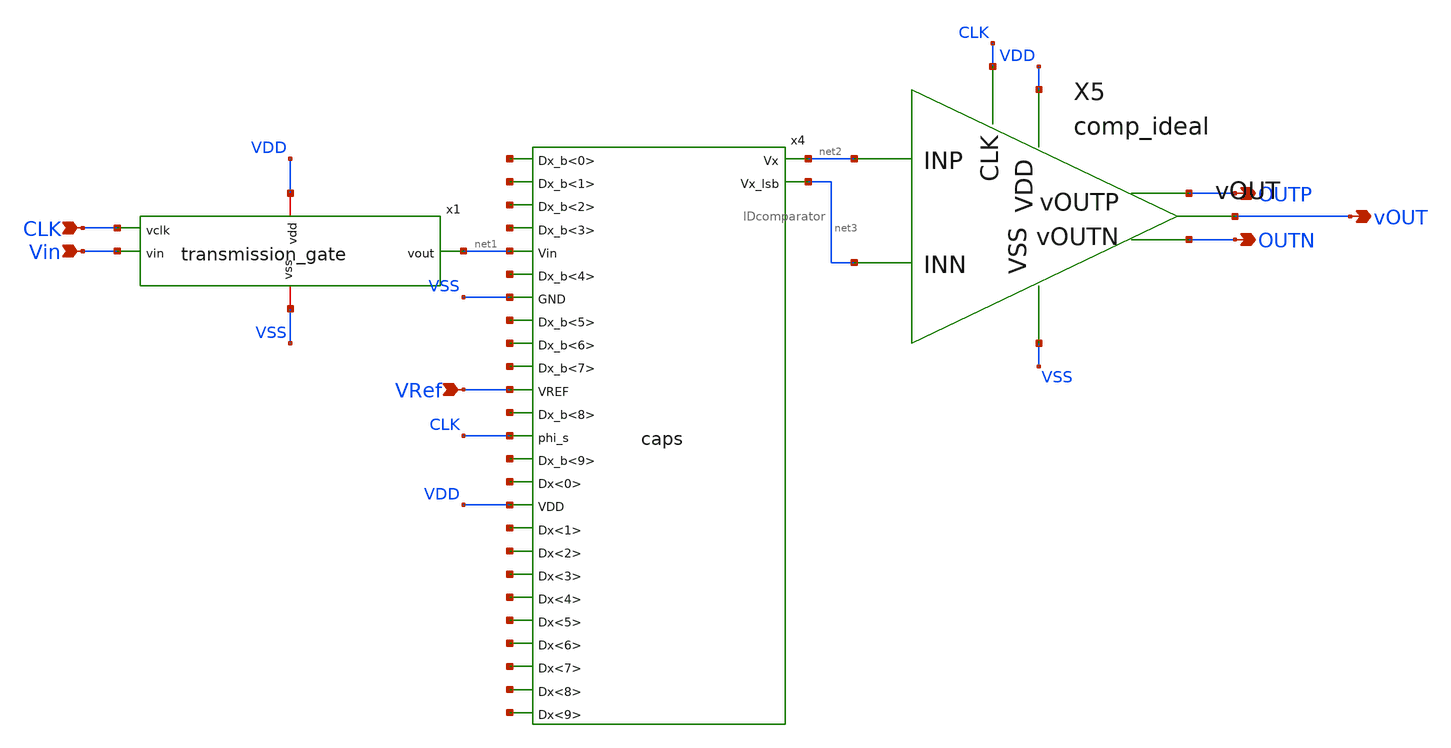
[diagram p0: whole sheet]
** sch_path: analog/top/top.sch
**.subckt top Vin CLK VRef OUTP OUTN vOUT
*.ipin Vin
*.ipin CLK
*.ipin VRef
*.opin OUTP
*.opin OUTN
*.opin vOUT
x4 net4 net5 net6 net7 net1 net8 VSS net9 net10 net11 VRef net12 CLK net13 net14 VDD net15 net2
+ net16 net17 net3 net18 net19 net20 net21 net22 net23 caps
X5 net2 net3 CLK VDD VSS OUTP OUTN vOUT comp_ideal
x1 VDD net1 CLK Vin VSS transmission_gate
**.ends
.end
